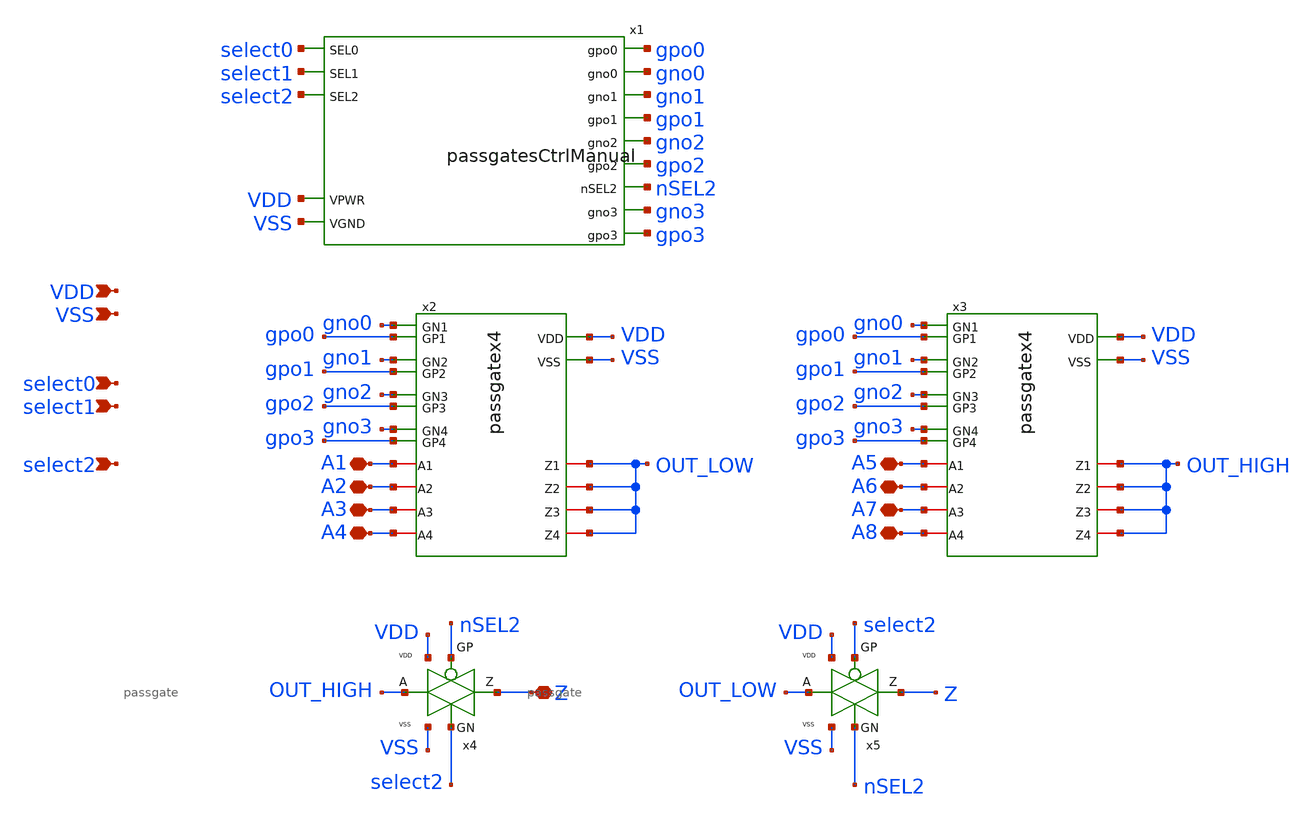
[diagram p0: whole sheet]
** sch_path: xschem/mux8to1.sch
**.subckt mux8to1 select0 select1 select2 VDD VSS Z A1 A2 A3 A4 A5 A6 A7 A8
*.ipin select0
*.ipin select1
*.ipin select2
*.ipin VDD
*.ipin VSS
*.iopin Z
*.iopin A1
*.iopin A2
*.iopin A3
*.iopin A4
*.iopin A5
*.iopin A6
*.iopin A7
*.iopin A8
x4 OUT_HIGH select2 nSEL2 Z VDD VSS passgate
x5 OUT_LOW nSEL2 select2 Z VDD VSS passgate
x2 A1 gno0 gpo0 OUT_LOW A2 gno1 gpo1 OUT_LOW A3 gno2 gpo2 OUT_LOW A4 gno3 gpo3 OUT_LOW VDD VSS
+ passgatex4
x1 select0 select1 select2 gno0 gpo0 gno1 gpo1 gno2 gpo2 gno3 gpo3 nSEL2 VDD VSS passgatesCtrlManual
x3 A5 gno0 gpo0 OUT_HIGH A6 gno1 gpo1 OUT_HIGH A7 gno2 gpo2 OUT_HIGH A8 gno3 gpo3 OUT_HIGH VDD VSS
+ passgatex4
**.ends

* expanding   symbol:  passgate.sym # of pins=6
** sym_path: xschem/passgate.sym
** sch_path: xschem/passgate.sch
.subckt passgate A GN GP Z VDD VSS
*.ipin GN
*.ipin VDD
*.ipin VSS
*.ipin GP
*.iopin A
*.iopin Z
XM1 Z GN A VSS sky130_fd_pr__nfet_01v8_lvt L=0.35 W=8 nf=1 ad='int((nf+1)/2) * W/nf * 0.29' as='int((nf+2)/2) * W/nf * 0.29'
+ pd='2*int((nf+1)/2) * (W/nf + 0.29)' ps='2*int((nf+2)/2) * (W/nf + 0.29)' nrd='0.29 / W' nrs='0.29 / W'
+ sa=0 sb=0 sd=0 mult=2 m=2
XM3 Z GP A VDD sky130_fd_pr__pfet_01v8_lvt L=0.35 W=10 nf=1 ad='int((nf+1)/2) * W/nf * 0.29' as='int((nf+2)/2) * W/nf * 0.29'
+ pd='2*int((nf+1)/2) * (W/nf + 0.29)' ps='2*int((nf+2)/2) * (W/nf + 0.29)' nrd='0.29 / W' nrs='0.29 / W'
+ sa=0 sb=0 sd=0 mult=2 m=2
.ends


* expanding   symbol:  passgatex4.sym # of pins=18
** sym_path: xschem/passgatex4.sym
** sch_path: xschem/passgatex4.sch
.subckt passgatex4 A1 GN1 GP1 Z1 A2 GN2 GP2 Z2 A3 GN3 GP3 Z3 A4 GN4 GP4 Z4 VDD VSS
*.ipin VDD
*.ipin VSS
*.ipin GP1
*.ipin GN1
*.iopin A1
*.iopin Z1
*.ipin GP2
*.ipin GN2
*.iopin A2
*.iopin Z2
*.ipin GP3
*.ipin GN3
*.iopin A3
*.iopin Z3
*.ipin GP4
*.ipin GN4
*.iopin A4
*.iopin Z4
x1 A1 GN1 GP1 Z1 VDD VSS passgate
x2 A2 GN2 GP2 Z2 VDD VSS passgate
x3 A3 GN3 GP3 Z3 VDD VSS passgate
x4 A4 GN4 GP4 Z4 VDD VSS passgate
.ends


* expanding   symbol:  passgatesCtrlManual.sym # of pins=14
** sym_path: xschem/passgatesCtrlManual.sym
** sch_path: xschem/passgatesCtrlManual.sch
.subckt passgatesCtrlManual SEL0 SEL1 SEL2 gno0 gpo0 gno1 gpo1 gno2 gpo2 gno3 gpo3 nSEL2 VPWR VGND
*.ipin SEL0
*.ipin SEL1
*.ipin SEL2
*.opin gno0
*.opin gpo0
*.opin gno1
*.opin gpo1
*.opin gno2
*.opin gpo2
*.opin gno3
*.opin gpo3
*.opin nSEL2
*.ipin VPWR
*.ipin VGND
x1 SEL0 VGND VGND VPWR VPWR nSEL0 sky130_fd_sc_hd__inv_2
x2 SEL1 VGND VGND VPWR VPWR nSEL1 sky130_fd_sc_hd__inv_2
x7 nSEL0 nSEL1 VGND VGND VPWR VPWR gno0 sky130_fd_sc_hd__and2_1
x10 SEL1 SEL0 VGND VGND VPWR VPWR gno3 sky130_fd_sc_hd__and2_1
x11 gno0 VGND VGND VPWR VPWR gpo0 sky130_fd_sc_hd__inv_2
x12 gno1 VGND VGND VPWR VPWR gpo1 sky130_fd_sc_hd__inv_2
x13 gno2 VGND VGND VPWR VPWR gpo2 sky130_fd_sc_hd__inv_2
x14 gno3 VGND VGND VPWR VPWR gpo3 sky130_fd_sc_hd__inv_2
x15 VGND VGND VPWR VPWR sky130_fd_sc_hd__decap_4
x16 VGND VGND VPWR VPWR sky130_fd_sc_hd__decap_4
x17 VGND VGND VPWR VPWR sky130_fd_sc_hd__decap_4
x8 SEL1 SEL0 VGND VGND VPWR VPWR gno1 sky130_fd_sc_hd__and2b_1
x9 SEL0 SEL1 VGND VGND VPWR VPWR gno2 sky130_fd_sc_hd__and2b_1
x18 SEL2 VGND VGND VPWR VPWR nSEL2 sky130_fd_sc_hd__inv_2
x19 VGND VGND VPWR VPWR sky130_fd_sc_hd__decap_4
.ends

.end
